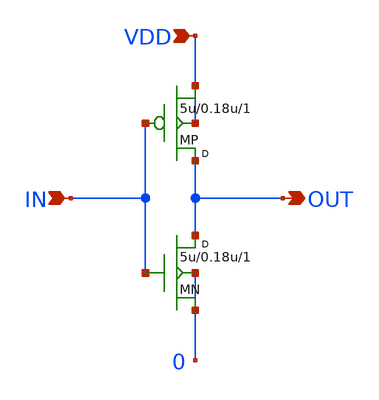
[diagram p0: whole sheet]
** sch_path: xschem_libraries_oa/ngspice_verilog_cosim/ainv/schematic/ainv.sch
**.subckt ainv IN OUT VDD
*.ipin IN
*.opin OUT
*.ipin VDD
MN OUT IN 0 0 N1
MP OUT IN VDD VDD P1
**.ends
**** begin user architecture code
.model n1 nmos   level=2 vto=0.5 kp=24e-6 gamma=0.15 phi=0.65 lambda=0.015 xj=0.5e-6

.model p1 pmos   level=2 vto=-0.5 kp=8.5e-6 gamma=0.4 phi=0.65 lambda=0.05 xj=0.5e-6

**** end user architecture code
.end
